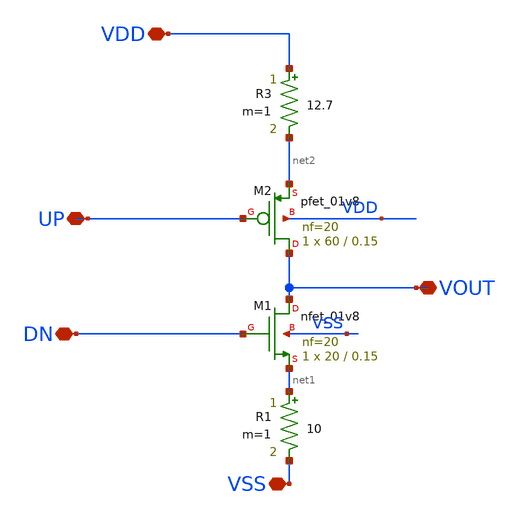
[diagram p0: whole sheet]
** sch_path: xschem/DC_DC_Converter_xschem/OTHERS/DC_DC_Converter_JV11/current_pump/current_pump_for_symbol.sch
**.subckt current_pump_for_symbol VDD UP DN VSS VOUT
*.iopin VDD
*.iopin UP
*.iopin DN
*.iopin VSS
*.iopin VOUT
R3 VDD net2 12.7 m=1
R1 net1 VSS 10 m=1
XM1 VOUT DN net1 VSS sky130_fd_pr__nfet_01v8 L=0.15 W=20 nf=20 ad='int((nf+1)/2) * W/nf * 0.29' as='int((nf+2)/2) * W/nf * 0.29'
+ pd='2*int((nf+1)/2) * (W/nf + 0.29)' ps='2*int((nf+2)/2) * (W/nf + 0.29)' nrd='0.29 / W' nrs='0.29 / W'
+ sa=0 sb=0 sd=0 mult=1 m=1
XM2 VOUT UP net2 VDD sky130_fd_pr__pfet_01v8 L=0.15 W=60 nf=20 ad='int((nf+1)/2) * W/nf * 0.29' as='int((nf+2)/2) * W/nf * 0.29'
+ pd='2*int((nf+1)/2) * (W/nf + 0.29)' ps='2*int((nf+2)/2) * (W/nf + 0.29)' nrd='0.29 / W' nrs='0.29 / W'
+ sa=0 sb=0 sd=0 mult=1 m=1
**.ends
.end
